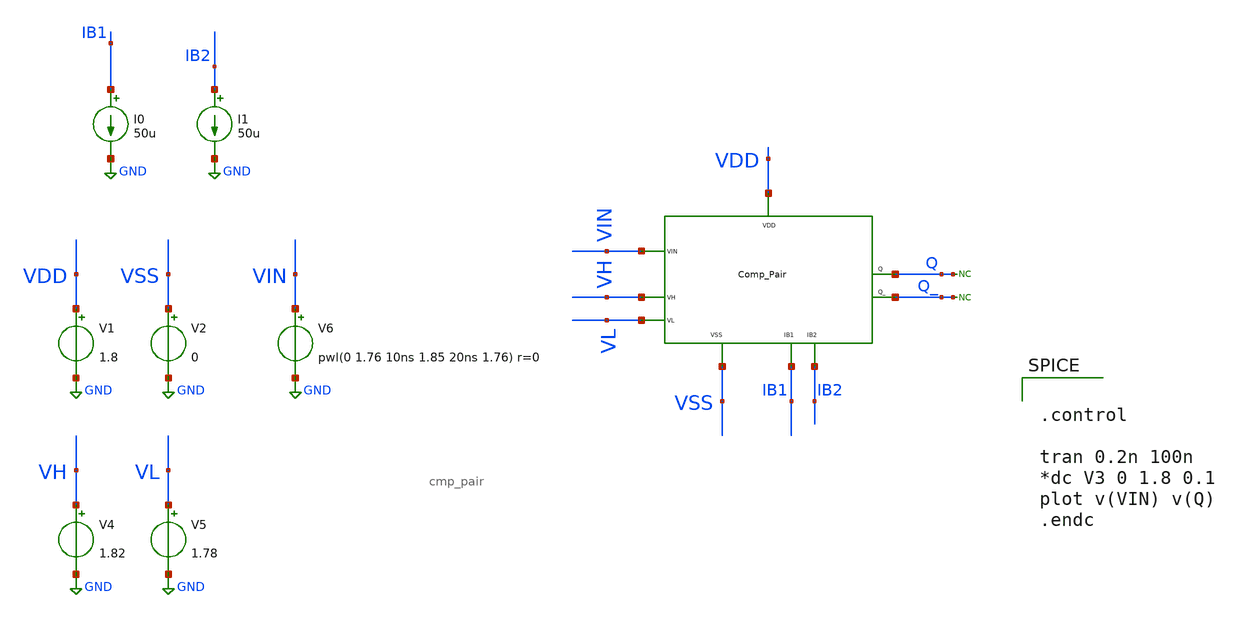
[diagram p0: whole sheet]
** sch_path: xschem/DC_DC_Converter_xschem/OTHERS/DC_DC_Converter_V7/Comparator_Pair/cmp_pair_tb.sch
**.subckt cmp_pair_tb
* noconn Q
* noconn Q_
V1 VDD GND 1.8
V2 VSS GND 0
V4 VH GND 1.82
V5 VL GND 1.78
I0 IB1 GND 50u
I1 IB2 GND 50u
V6 VIN GND pwl(0 1.76 10ns 1.85 20ns 1.76) r=0
XM1 VDD VSS VIN VH VL IB1 IB2 Q Q_ cmp_pair
**** begin user architecture code

** opencircuitdesign pdks install
.lib $::SKYWATER_MODELS/sky130.lib.spice tt




.control

tran 0.2n 100n
*dc V3 0 1.8 0.1
plot v(VIN) v(Q)
.endc


**** end user architecture code
**.ends

* expanding   symbol:  DC_DC_Converter/Comparator_Pair/cmp_pair.sym # of pins=9
** sym_path: xschem/DC_DC_Converter_xschem/OTHERS/DC_DC_Converter_V7/Comparator_Pair/cmp_pair.sym
** sch_path: xschem/DC_DC_Converter_xschem/OTHERS/DC_DC_Converter_V7/Comparator_Pair/cmp_pair.sch
.subckt cmp_pair VDD VSS VIN VH VL IB1 IB2 Q Q_
*.iopin VDD
*.iopin VSS
*.iopin IB1
*.iopin IB2
*.iopin VH
*.iopin VL
*.iopin Q
*.iopin Q_
*.iopin VIN
XM1 IB1 VDD VH VIN VSS Q Comparator
XM2 IB2 VDD VIN VL VSS Q_ Comparator
.ends


* expanding   symbol:  DC_DC_Converter/Comparator/Comparator.sym # of pins=6
** sym_path: xschem/DC_DC_Converter_xschem/OTHERS/DC_DC_Converter_V7/Comparator/Comparator.sym
** sch_path: xschem/DC_DC_Converter_xschem/OTHERS/DC_DC_Converter_V7/Comparator/Comparator.sch
.subckt Comparator IBIAS VDD IN_P IN_N VSS OUT
*.iopin VDD
*.iopin VSS
*.iopin IN_P
*.iopin IN_N
*.iopin OUT
*.iopin IBIAS
XM15 1_N IN_P IBIAS VSS sky130_fd_pr__nfet_01v8 L=1 W=5 nf=1 ad='int((nf+1)/2) * W/nf * 0.29' as='int((nf+2)/2) * W/nf * 0.29'
+ pd='2*int((nf+1)/2) * (W/nf + 0.29)' ps='2*int((nf+2)/2) * (W/nf + 0.29)' nrd='0.29 / W' nrs='0.29 / W'
+ sa=0 sb=0 sd=0 mult=1 m=1
XM1 1_P IN_N IBIAS VSS sky130_fd_pr__nfet_01v8 L=1 W=5 nf=1 ad='int((nf+1)/2) * W/nf * 0.29' as='int((nf+2)/2) * W/nf * 0.29'
+ pd='2*int((nf+1)/2) * (W/nf + 0.29)' ps='2*int((nf+2)/2) * (W/nf + 0.29)' nrd='0.29 / W' nrs='0.29 / W'
+ sa=0 sb=0 sd=0 mult=1 m=1
XM2 2_P 2_P VSS VSS sky130_fd_pr__nfet_01v8 L=2 W=2 nf=1 ad='int((nf+1)/2) * W/nf * 0.29' as='int((nf+2)/2) * W/nf * 0.29'
+ pd='2*int((nf+1)/2) * (W/nf + 0.29)' ps='2*int((nf+2)/2) * (W/nf + 0.29)' nrd='0.29 / W' nrs='0.29 / W'
+ sa=0 sb=0 sd=0 mult=1 m=1
XM10 2_N 2_P VSS VSS sky130_fd_pr__nfet_01v8 L=2 W=2 nf=1 ad='int((nf+1)/2) * W/nf * 0.29' as='int((nf+2)/2) * W/nf * 0.29'
+ pd='2*int((nf+1)/2) * (W/nf + 0.29)' ps='2*int((nf+2)/2) * (W/nf + 0.29)' nrd='0.29 / W' nrs='0.29 / W'
+ sa=0 sb=0 sd=0 mult=1 m=1
XM11 OP_1 2_N VSS VSS sky130_fd_pr__nfet_01v8 L=1 W=1 nf=1 ad='int((nf+1)/2) * W/nf * 0.29' as='int((nf+2)/2) * W/nf * 0.29'
+ pd='2*int((nf+1)/2) * (W/nf + 0.29)' ps='2*int((nf+2)/2) * (W/nf + 0.29)' nrd='0.29 / W' nrs='0.29 / W'
+ sa=0 sb=0 sd=0 mult=1 m=1
XM13 OUT OP_1 VSS VSS sky130_fd_pr__nfet_01v8 L=1 W=1 nf=1 ad='int((nf+1)/2) * W/nf * 0.29' as='int((nf+2)/2) * W/nf * 0.29'
+ pd='2*int((nf+1)/2) * (W/nf + 0.29)' ps='2*int((nf+2)/2) * (W/nf + 0.29)' nrd='0.29 / W' nrs='0.29 / W'
+ sa=0 sb=0 sd=0 mult=1 m=1
XM9 2_P 1_N VDD VDD sky130_fd_pr__pfet_01v8 L=0.5 W=1 nf=1 ad='int((nf+1)/2) * W/nf * 0.29' as='int((nf+2)/2) * W/nf * 0.29'
+ pd='2*int((nf+1)/2) * (W/nf + 0.29)' ps='2*int((nf+2)/2) * (W/nf + 0.29)' nrd='0.29 / W' nrs='0.29 / W'
+ sa=0 sb=0 sd=0 mult=1 m=1
XM6 1_N 1_N VDD VDD sky130_fd_pr__pfet_01v8 L=0.5 W=1.5 nf=1 ad='int((nf+1)/2) * W/nf * 0.29' as='int((nf+2)/2) * W/nf * 0.29'
+ pd='2*int((nf+1)/2) * (W/nf + 0.29)' ps='2*int((nf+2)/2) * (W/nf + 0.29)' nrd='0.29 / W' nrs='0.29 / W'
+ sa=0 sb=0 sd=0 mult=1 m=1
XM4 1_N 1_P VDD VDD sky130_fd_pr__pfet_01v8 L=0.5 W=1.5 nf=1 ad='int((nf+1)/2) * W/nf * 0.29' as='int((nf+2)/2) * W/nf * 0.29'
+ pd='2*int((nf+1)/2) * (W/nf + 0.29)' ps='2*int((nf+2)/2) * (W/nf + 0.29)' nrd='0.29 / W' nrs='0.29 / W'
+ sa=0 sb=0 sd=0 mult=1 m=1
XM3 1_P 1_N VDD VDD sky130_fd_pr__pfet_01v8 L=0.5 W=1.5 nf=1 ad='int((nf+1)/2) * W/nf * 0.29' as='int((nf+2)/2) * W/nf * 0.29'
+ pd='2*int((nf+1)/2) * (W/nf + 0.29)' ps='2*int((nf+2)/2) * (W/nf + 0.29)' nrd='0.29 / W' nrs='0.29 / W'
+ sa=0 sb=0 sd=0 mult=1 m=1
XM5 1_P 1_P VDD VDD sky130_fd_pr__pfet_01v8 L=0.5 W=1.5 nf=1 ad='int((nf+1)/2) * W/nf * 0.29' as='int((nf+2)/2) * W/nf * 0.29'
+ pd='2*int((nf+1)/2) * (W/nf + 0.29)' ps='2*int((nf+2)/2) * (W/nf + 0.29)' nrd='0.29 / W' nrs='0.29 / W'
+ sa=0 sb=0 sd=0 mult=1 m=1
XM7 2_N 1_P VDD VDD sky130_fd_pr__pfet_01v8 L=0.5 W=1 nf=1 ad='int((nf+1)/2) * W/nf * 0.29' as='int((nf+2)/2) * W/nf * 0.29'
+ pd='2*int((nf+1)/2) * (W/nf + 0.29)' ps='2*int((nf+2)/2) * (W/nf + 0.29)' nrd='0.29 / W' nrs='0.29 / W'
+ sa=0 sb=0 sd=0 mult=1 m=1
XM8 OP_1 2_N VDD VDD sky130_fd_pr__pfet_01v8 L=1 W=2.5 nf=1 ad='int((nf+1)/2) * W/nf * 0.29' as='int((nf+2)/2) * W/nf * 0.29'
+ pd='2*int((nf+1)/2) * (W/nf + 0.29)' ps='2*int((nf+2)/2) * (W/nf + 0.29)' nrd='0.29 / W' nrs='0.29 / W'
+ sa=0 sb=0 sd=0 mult=1 m=1
XM12 OUT OP_1 VDD VDD sky130_fd_pr__pfet_01v8 L=1 W=2.5 nf=1 ad='int((nf+1)/2) * W/nf * 0.29' as='int((nf+2)/2) * W/nf * 0.29'
+ pd='2*int((nf+1)/2) * (W/nf + 0.29)' ps='2*int((nf+2)/2) * (W/nf + 0.29)' nrd='0.29 / W' nrs='0.29 / W'
+ sa=0 sb=0 sd=0 mult=1 m=1
.ends

.GLOBAL GND
.end
